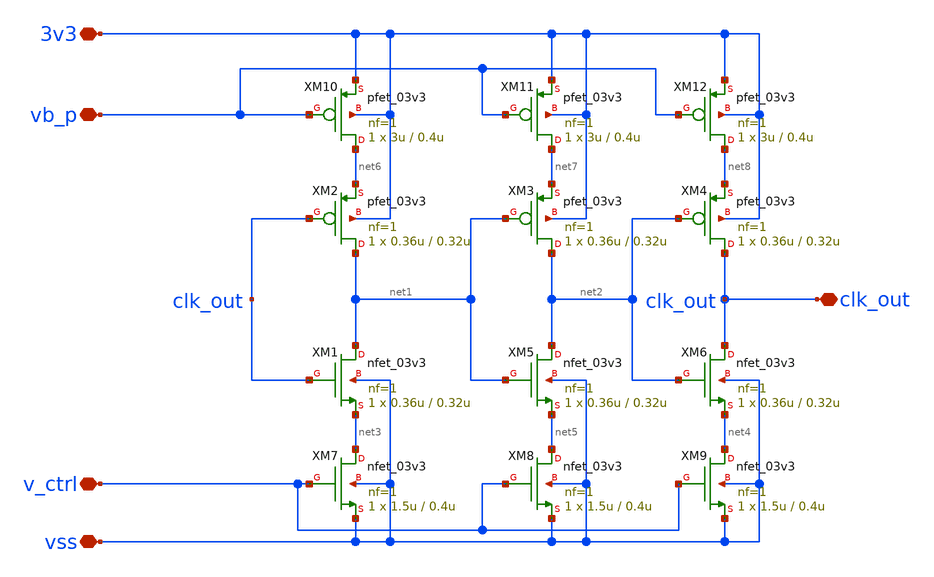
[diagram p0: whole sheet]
** sch_path: PLL/analog/schematics/Ring_Oscillator_Block.sch
* Copyright 2022 GlobalFoundries PDK Authors
* Licensed under the Apache License, Version 2.0 (the "License");
* you may not use this file except in compliance with the License.
* You may obtain a copy of the License at
* https://www.apache.org/licenses/LICENSE-2.0
* Unless required by applicable law or agreed to in writing, software
* distributed under the License is distributed on an "AS IS" BASIS,
* WITHOUT WARRANTIES OR CONDITIONS OF ANY KIND, either express or implied.
* See the License for the specific language governing permissions and
* limitations under the License.
**.subckt Ring_Oscillator_Block 3v3 vb_p clk_out v_ctrl vss
*.iopin 3v3
*.iopin vb_p
*.iopin clk_out
*.iopin v_ctrl
*.iopin vss
XM1 net1 clk_out net3 vss nfet_03v3 L=0.32u W=0.36u nf=1 ad='int((nf+1)/2) * W/nf * 0.18u' as='int((nf+2)/2) * W/nf * 0.18u'
+ pd='2*int((nf+1)/2) * (W/nf + 0.18u)' ps='2*int((nf+2)/2) * (W/nf + 0.18u)' nrd='0.18u / W' nrs='0.18u / W'
+ sa=0 sb=0 sd=0 m=1
XM2 net1 clk_out net6 3v3 pfet_03v3 L=0.32u W=0.36u nf=1 ad='int((nf+1)/2) * W/nf * 0.18u' as='int((nf+2)/2) * W/nf * 0.18u'
+ pd='2*int((nf+1)/2) * (W/nf + 0.18u)' ps='2*int((nf+2)/2) * (W/nf + 0.18u)' nrd='0.18u / W' nrs='0.18u / W'
+ sa=0 sb=0 sd=0 m=1
XM3 net2 net1 net7 3v3 pfet_03v3 L=0.32u W=0.36u nf=1 ad='int((nf+1)/2) * W/nf * 0.18u' as='int((nf+2)/2) * W/nf * 0.18u'
+ pd='2*int((nf+1)/2) * (W/nf + 0.18u)' ps='2*int((nf+2)/2) * (W/nf + 0.18u)' nrd='0.18u / W' nrs='0.18u / W'
+ sa=0 sb=0 sd=0 m=1
XM4 clk_out net2 net8 3v3 pfet_03v3 L=0.32u W=0.36u nf=1 ad='int((nf+1)/2) * W/nf * 0.18u' as='int((nf+2)/2) * W/nf * 0.18u'
+ pd='2*int((nf+1)/2) * (W/nf + 0.18u)' ps='2*int((nf+2)/2) * (W/nf + 0.18u)' nrd='0.18u / W' nrs='0.18u / W'
+ sa=0 sb=0 sd=0 m=1
XM5 net2 net1 net5 vss nfet_03v3 L=0.32u W=0.36u nf=1 ad='int((nf+1)/2) * W/nf * 0.18u' as='int((nf+2)/2) * W/nf * 0.18u'
+ pd='2*int((nf+1)/2) * (W/nf + 0.18u)' ps='2*int((nf+2)/2) * (W/nf + 0.18u)' nrd='0.18u / W' nrs='0.18u / W'
+ sa=0 sb=0 sd=0 m=1
XM6 clk_out net2 net4 vss nfet_03v3 L=0.32u W=0.36u nf=1 ad='int((nf+1)/2) * W/nf * 0.18u' as='int((nf+2)/2) * W/nf * 0.18u'
+ pd='2*int((nf+1)/2) * (W/nf + 0.18u)' ps='2*int((nf+2)/2) * (W/nf + 0.18u)' nrd='0.18u / W' nrs='0.18u / W'
+ sa=0 sb=0 sd=0 m=1
XM7 net3 v_ctrl vss vss nfet_03v3 L=0.4u W=1.5u nf=1 ad='int((nf+1)/2) * W/nf * 0.18u' as='int((nf+2)/2) * W/nf * 0.18u'
+ pd='2*int((nf+1)/2) * (W/nf + 0.18u)' ps='2*int((nf+2)/2) * (W/nf + 0.18u)' nrd='0.18u / W' nrs='0.18u / W'
+ sa=0 sb=0 sd=0 m=1
XM8 net5 v_ctrl vss vss nfet_03v3 L=0.4u W=1.5u nf=1 ad='int((nf+1)/2) * W/nf * 0.18u' as='int((nf+2)/2) * W/nf * 0.18u'
+ pd='2*int((nf+1)/2) * (W/nf + 0.18u)' ps='2*int((nf+2)/2) * (W/nf + 0.18u)' nrd='0.18u / W' nrs='0.18u / W'
+ sa=0 sb=0 sd=0 m=1
XM9 net4 v_ctrl vss vss nfet_03v3 L=0.4u W=1.5u nf=1 ad='int((nf+1)/2) * W/nf * 0.18u' as='int((nf+2)/2) * W/nf * 0.18u'
+ pd='2*int((nf+1)/2) * (W/nf + 0.18u)' ps='2*int((nf+2)/2) * (W/nf + 0.18u)' nrd='0.18u / W' nrs='0.18u / W'
+ sa=0 sb=0 sd=0 m=1
XM10 net6 vb_p 3v3 3v3 pfet_03v3 L=0.4u W=3u nf=1 ad='int((nf+1)/2) * W/nf * 0.18u' as='int((nf+2)/2) * W/nf * 0.18u'
+ pd='2*int((nf+1)/2) * (W/nf + 0.18u)' ps='2*int((nf+2)/2) * (W/nf + 0.18u)' nrd='0.18u / W' nrs='0.18u / W'
+ sa=0 sb=0 sd=0 m=1
XM11 net7 vb_p 3v3 3v3 pfet_03v3 L=0.4u W=3u nf=1 ad='int((nf+1)/2) * W/nf * 0.18u' as='int((nf+2)/2) * W/nf * 0.18u'
+ pd='2*int((nf+1)/2) * (W/nf + 0.18u)' ps='2*int((nf+2)/2) * (W/nf + 0.18u)' nrd='0.18u / W' nrs='0.18u / W'
+ sa=0 sb=0 sd=0 m=1
XM12 net8 vb_p 3v3 3v3 pfet_03v3 L=0.4u W=3u nf=1 ad='int((nf+1)/2) * W/nf * 0.18u' as='int((nf+2)/2) * W/nf * 0.18u'
+ pd='2*int((nf+1)/2) * (W/nf + 0.18u)' ps='2*int((nf+2)/2) * (W/nf + 0.18u)' nrd='0.18u / W' nrs='0.18u / W'
+ sa=0 sb=0 sd=0 m=1
**.ends
.end
